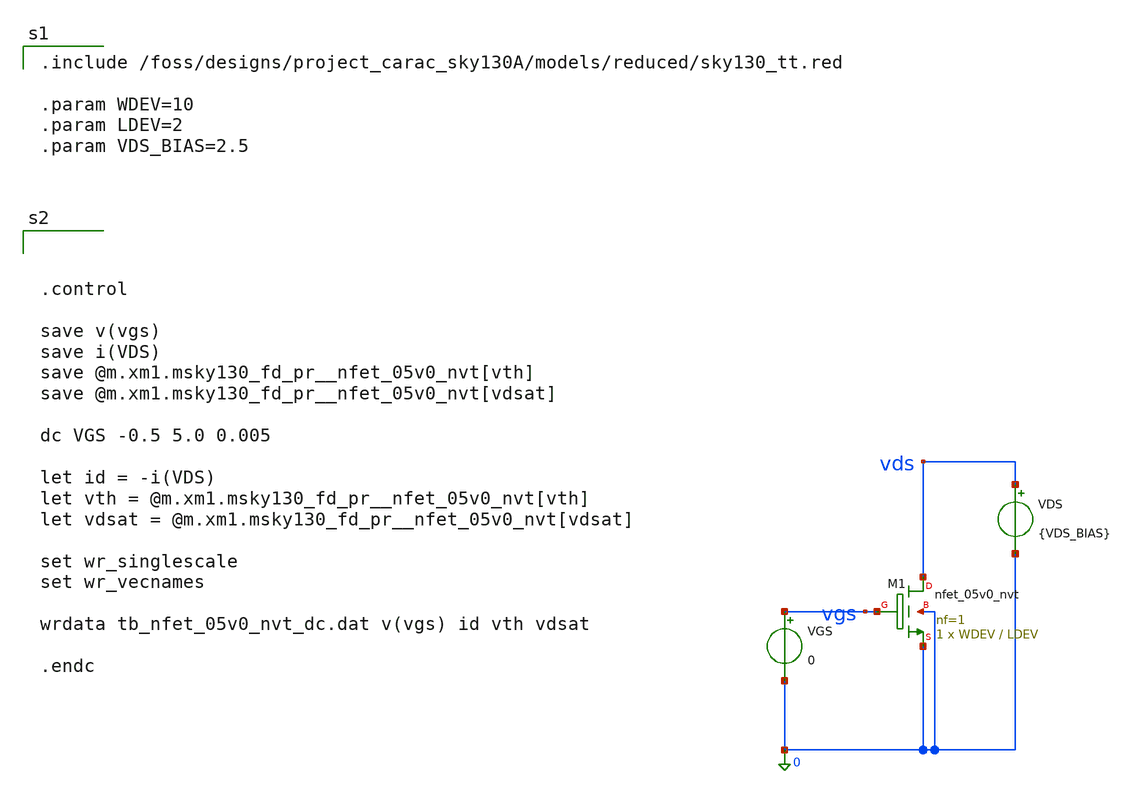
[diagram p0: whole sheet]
** sch_path: dfii/project_carac_sky130A_sim/tb_nfet_05v0_nvt_dc.sch
* Copyright 2021 Stefan Frederik Schippers
* Licensed under the Apache License, Version 2.0 (the "License");
* you may not use this file except in compliance with the License.
* You may obtain a copy of the License at
* https://www.apache.org/licenses/LICENSE-2.0
* Unless required by applicable law or agreed to in writing, software
* distributed under the License is distributed on an "AS IS" BASIS,
* WITHOUT WARRANTIES OR CONDITIONS OF ANY KIND, either express or implied.
* See the License for the specific language governing permissions and
* limitations under the License.

.include /foss/designs/project_carac_sky130A/models/reduced/sky130_tt.red

.param WDEV=10
.param LDEV=2
.param VDS_BIAS=2.5



**.subckt tb_nfet_05v0_nvt_dc
VGS vgs 0 0
VDS vds 0 {VDS_BIAS}
XM1 vds vgs 0 0 sky130_fd_pr__nfet_05v0_nvt L=LDEV W=WDEV nf=1 ad='int((1 + 1)/2) * WDEV / 1 * 0.29'
+ as='int((1 + 2)/2) * WDEV / 1 * 0.29' pd='2*int((1 + 1)/2) * (WDEV / 1 + 0.29)' ps='2*int((1 + 2)/2) * (WDEV / 1 + 0.29)'
+ nrd='0.29 / WDEV ' nrs='0.29 / WDEV ' sa=0 sb=0 sd=0 mult=1 m=1
**.ends
**** begin user architecture code



.control

save v(vgs)
save i(VDS)
save @m.xm1.msky130_fd_pr__nfet_05v0_nvt[vth]
save @m.xm1.msky130_fd_pr__nfet_05v0_nvt[vdsat]

dc VGS -0.5 5.0 0.005

let id = -i(VDS)
let vth = @m.xm1.msky130_fd_pr__nfet_05v0_nvt[vth]
let vdsat = @m.xm1.msky130_fd_pr__nfet_05v0_nvt[vdsat]

set wr_singlescale
set wr_vecnames

wrdata tb_nfet_05v0_nvt_dc.dat v(vgs) id vth vdsat

.endc

**** end user architecture code
.end
